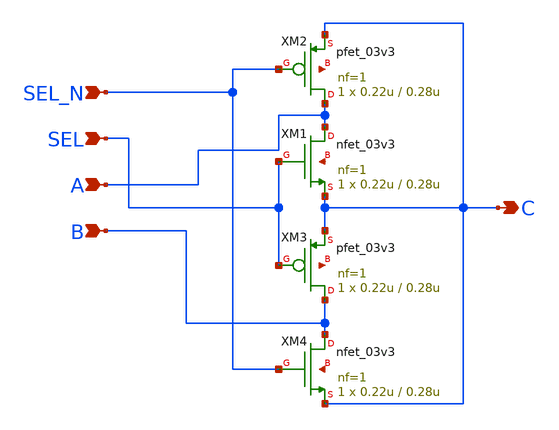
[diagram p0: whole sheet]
** sch_path: Chandra/mux_2to1_wo_single_select.sch
**.subckt mux_2to1_wo_single_select A B SEL C SEL_N
*.ipin A
*.ipin B
*.ipin SEL
*.opin C
*.ipin SEL_N
XM1 A SEL C net1 nfet_03v3 L=0.28u W=0.22u nf=1 ad='int((nf+1)/2) * W/nf * 0.18u' as='int((nf+2)/2) * W/nf * 0.18u'
+ pd='2*int((nf+1)/2) * (W/nf + 0.18u)' ps='2*int((nf+2)/2) * (W/nf + 0.18u)' nrd='0.18u / W' nrs='0.18u / W'
+ sa=0 sb=0 sd=0 m=1
XM2 A SEL_N C net2 pfet_03v3 L=0.28u W=0.22u nf=1 ad='int((nf+1)/2) * W/nf * 0.18u' as='int((nf+2)/2) * W/nf * 0.18u'
+ pd='2*int((nf+1)/2) * (W/nf + 0.18u)' ps='2*int((nf+2)/2) * (W/nf + 0.18u)' nrd='0.18u / W' nrs='0.18u / W'
+ sa=0 sb=0 sd=0 m=1
XM3 B SEL C net3 pfet_03v3 L=0.28u W=0.22u nf=1 ad='int((nf+1)/2) * W/nf * 0.18u' as='int((nf+2)/2) * W/nf * 0.18u'
+ pd='2*int((nf+1)/2) * (W/nf + 0.18u)' ps='2*int((nf+2)/2) * (W/nf + 0.18u)' nrd='0.18u / W' nrs='0.18u / W'
+ sa=0 sb=0 sd=0 m=1
XM4 B SEL_N C net4 nfet_03v3 L=0.28u W=0.22u nf=1 ad='int((nf+1)/2) * W/nf * 0.18u' as='int((nf+2)/2) * W/nf * 0.18u'
+ pd='2*int((nf+1)/2) * (W/nf + 0.18u)' ps='2*int((nf+2)/2) * (W/nf + 0.18u)' nrd='0.18u / W' nrs='0.18u / W'
+ sa=0 sb=0 sd=0 m=1
**.ends
.end
